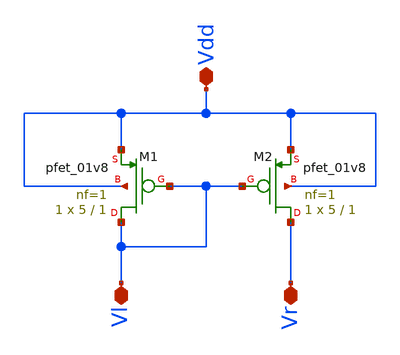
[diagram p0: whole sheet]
** sch_path: Circuits/DiffAmp/PMOS_Load.sch
**.subckt PMOS_Load Vdd Vl Vr
*.iopin Vdd
*.iopin Vl
*.iopin Vr
XM1 Vl Vl Vdd Vdd sky130_fd_pr__pfet_01v8 L=1 W=5 nf=1 ad='int((nf+1)/2) * W/nf * 0.29' as='int((nf+2)/2) * W/nf * 0.29'
+ pd='2*int((nf+1)/2) * (W/nf + 0.29)' ps='2*int((nf+2)/2) * (W/nf + 0.29)' nrd='0.29 / W' nrs='0.29 / W'
+ sa=0 sb=0 sd=0 mult=1 m=1
XM2 Vr Vl Vdd Vdd sky130_fd_pr__pfet_01v8 L=1 W=5 nf=1 ad='int((nf+1)/2) * W/nf * 0.29' as='int((nf+2)/2) * W/nf * 0.29'
+ pd='2*int((nf+1)/2) * (W/nf + 0.29)' ps='2*int((nf+2)/2) * (W/nf + 0.29)' nrd='0.29 / W' nrs='0.29 / W'
+ sa=0 sb=0 sd=0 mult=1 m=1
**.ends
.end
